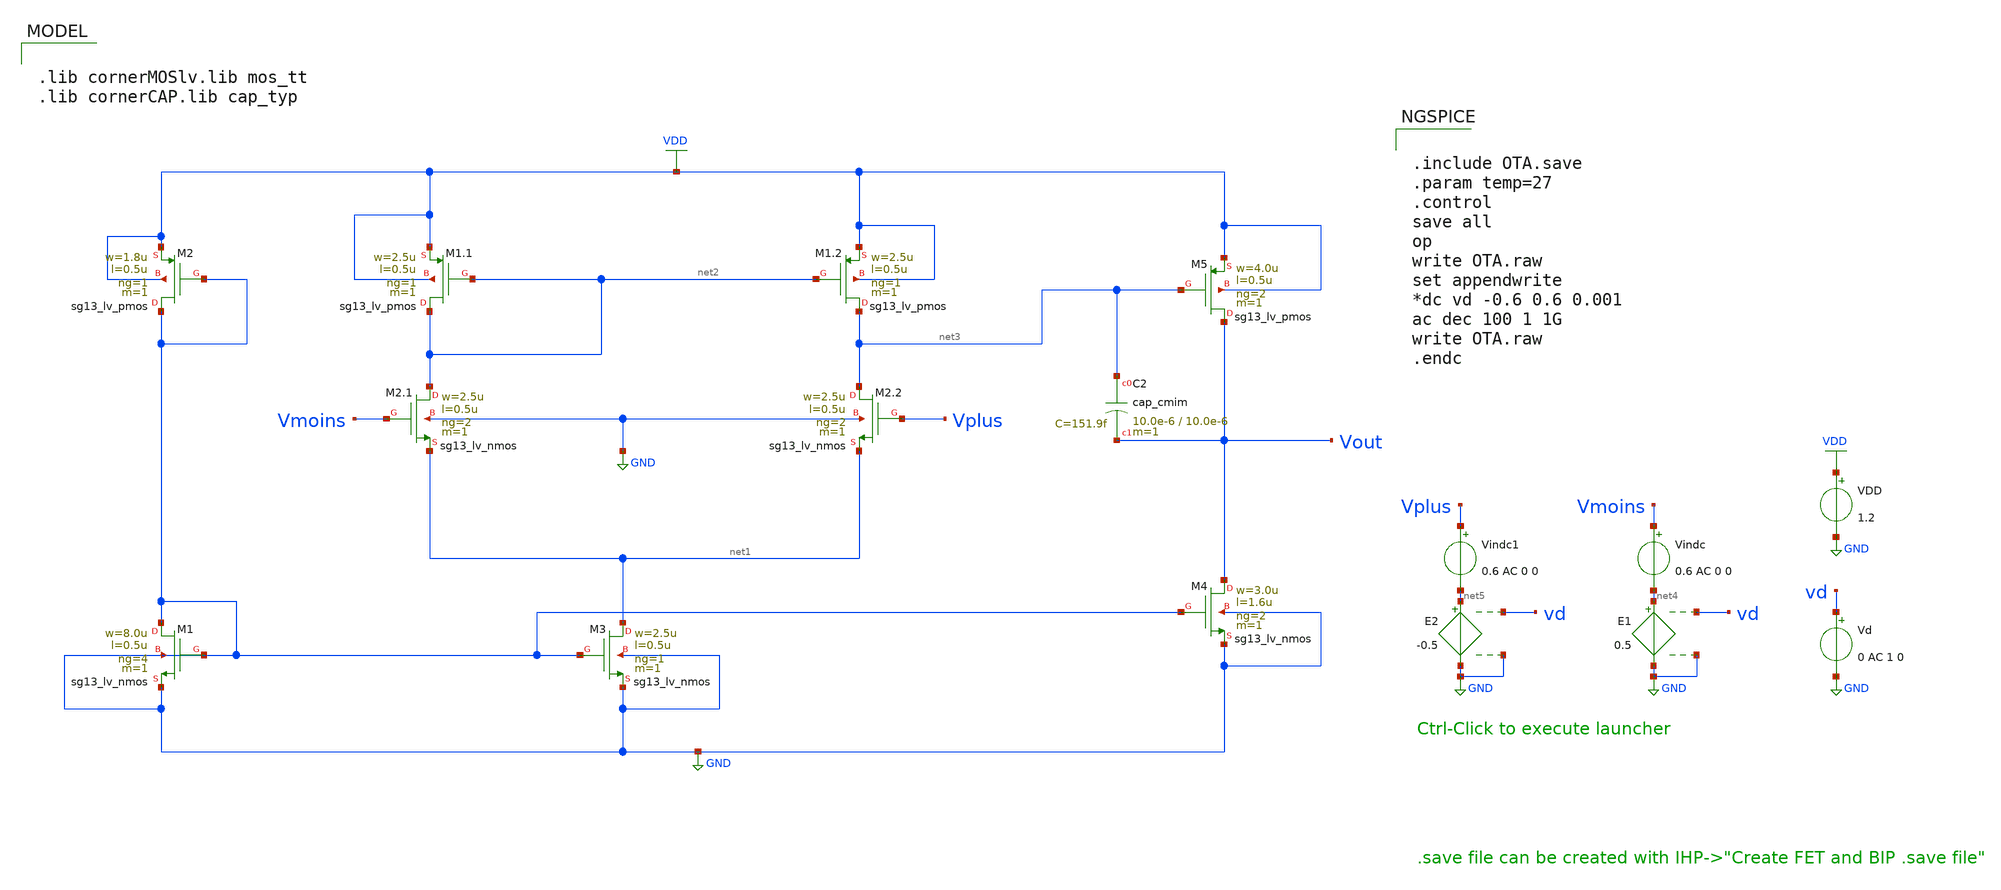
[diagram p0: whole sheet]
** sch_path: dc_lv_nmos.sch
* Copyright 2023 IHP PDK Authors
**.subckt dc_lv_nmos
XM3 net1 GND GND GND sg13_lv_nmos w=2.5u l=0.5u ng=1 m=1 mm_ok=1
XM2.1 net2 Vmoins net1 GND sg13_lv_nmos w=2.5u l=0.5u ng=2 m=1 mm_ok=1
XM2.2 net3 Vplus net1 GND sg13_lv_nmos w=2.5u l=0.5u ng=2 m=1 mm_ok=1
XM1.1 net2 net2 VDD VDD sg13_lv_pmos w=2.5u l=0.5u ng=1 m=1 mm_ok=1
XM1.2 net3 net2 VDD VDD sg13_lv_pmos w=2.5u l=0.5u ng=1 m=1 mm_ok=1
XM4 Vout GND GND GND sg13_lv_nmos w=3.0u l=1.6u ng=2 m=1 mm_ok=1
XM5 Vout net3 VDD VDD sg13_lv_pmos w=4.0u l=0.5u ng=2 m=1 mm_ok=1
XC2 net3 Vout cap_cmim w=10.0e-6 l=10.0e-6 m=1 mm_ok=1
XM1 GND GND GND GND sg13_lv_nmos w=8.0u l=0.5u ng=4 m=1 mm_ok=1
XM2 GND GND VDD VDD sg13_lv_pmos w=1.8u l=0.5u ng=1 m=1 mm_ok=1
Vindc Vmoins net4 0.6 AC 0 0
Vd vd GND 0 AC 1 0
E1 net4 GND vd GND 0.5
Vindc1 Vplus net5 0.6 AC 0 0
E2 net5 GND vd GND -0.5
VDD VDD GND 1.2
**** begin user architecture code


.include OTA.save
.param temp=27
.control
save all
op
write OTA.raw
set appendwrite
*dc vd -0.6 0.6 0.001
ac dec 100 1 1G
write OTA.raw
.endc



.lib cornerMOSlv.lib mos_tt
.lib cornerCAP.lib cap_typ

**** end user architecture code
**.ends
.GLOBAL GND
.GLOBAL VDD
.end
